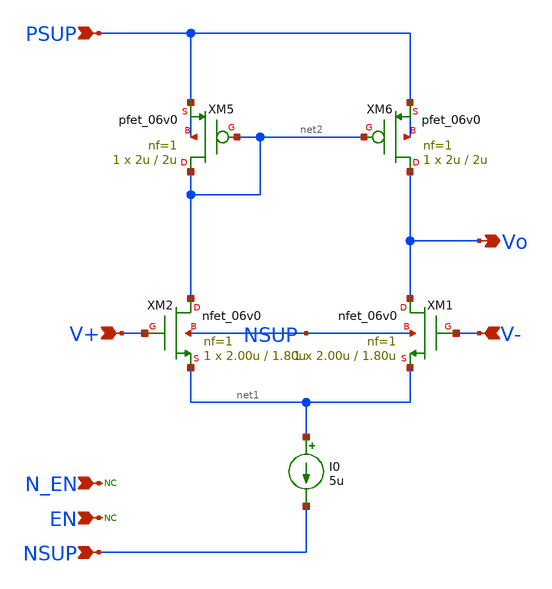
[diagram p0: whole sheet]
** sch_path: xschem/blocks/aux_amp/aux_amp.sch
**.subckt aux_amp PSUP NSUP N_EN EN V+ V- Vo
*.ipin PSUP
*.ipin NSUP
*.ipin N_EN
*.ipin EN
*.ipin V+
*.ipin V-
*.opin Vo
XM5 net2 net2 PSUP PSUP pfet_06v0 L=2u W=2u nf=1 ad='int((nf+1)/2) * W/nf * 0.18u' as='int((nf+2)/2) * W/nf * 0.18u'
+ pd='2*int((nf+1)/2) * (W/nf + 0.18u)' ps='2*int((nf+2)/2) * (W/nf + 0.18u)' nrd='0.18u / W' nrs='0.18u / W'
+ sa=0 sb=0 sd=0 m=1
XM6 Vo net2 PSUP PSUP pfet_06v0 L=2u W=2u nf=1 ad='int((nf+1)/2) * W/nf * 0.18u' as='int((nf+2)/2) * W/nf * 0.18u'
+ pd='2*int((nf+1)/2) * (W/nf + 0.18u)' ps='2*int((nf+2)/2) * (W/nf + 0.18u)' nrd='0.18u / W' nrs='0.18u / W'
+ sa=0 sb=0 sd=0 m=1
I0 net1 NSUP 5u
* noconn N_EN
* noconn EN
XM1 Vo V- net1 NSUP nfet_06v0 L=1.80u W=2.00u nf=1 ad='int((nf+1)/2) * W/nf * 0.18u' as='int((nf+2)/2) * W/nf * 0.18u'
+ pd='2*int((nf+1)/2) * (W/nf + 0.18u)' ps='2*int((nf+2)/2) * (W/nf + 0.18u)' nrd='0.18u / W' nrs='0.18u / W'
+ sa=0 sb=0 sd=0 m=1
XM2 net2 V+ net1 NSUP nfet_06v0 L=1.80u W=2.00u nf=1 ad='int((nf+1)/2) * W/nf * 0.18u' as='int((nf+2)/2) * W/nf * 0.18u'
+ pd='2*int((nf+1)/2) * (W/nf + 0.18u)' ps='2*int((nf+2)/2) * (W/nf + 0.18u)' nrd='0.18u / W' nrs='0.18u / W'
+ sa=0 sb=0 sd=0 m=1
**.ends
.end
